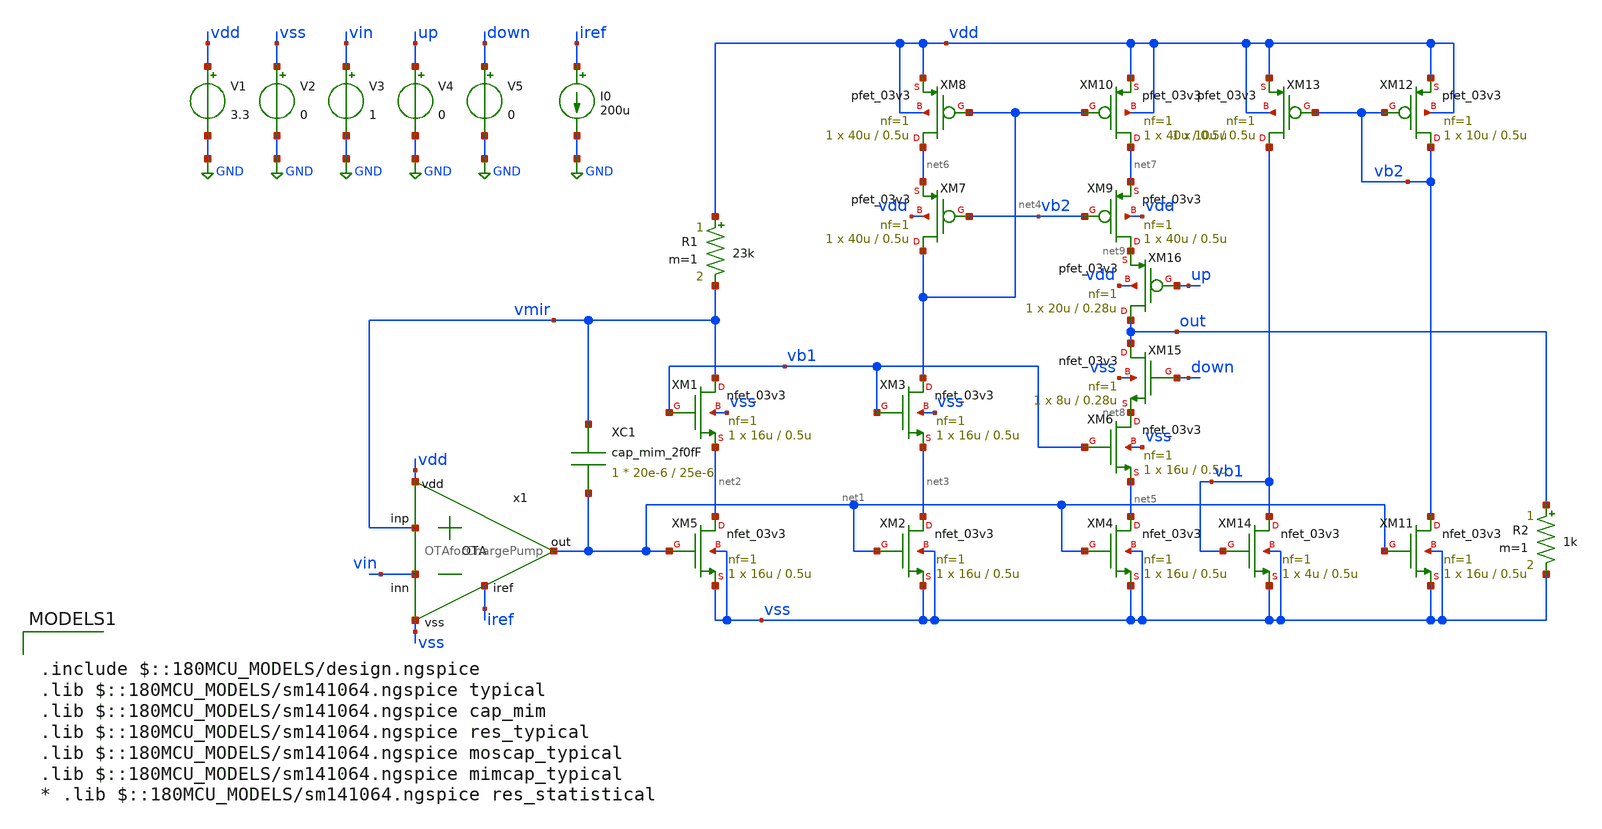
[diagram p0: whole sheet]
** sch_path: designs/libs/qw_core_analog_pkedit/VCOCP/VCOCP.sch
**.subckt VCOCP
x1 vdd iref vmir vin net1 vss OTAforChargePump
XM5 net2 net1 vss vss nfet_03v3 L=0.5u W=16u nf=1 ad='int((nf+1)/2) * W/nf * 0.18u' as='int((nf+2)/2) * W/nf * 0.18u'
+ pd='2*int((nf+1)/2) * (W/nf + 0.18u)' ps='2*int((nf+2)/2) * (W/nf + 0.18u)' nrd='0.18u / W' nrs='0.18u / W'
+ sa=0 sb=0 sd=0 m=1
XM1 vmir vb1 net2 vss nfet_03v3 L=0.5u W=16u nf=1 ad='int((nf+1)/2) * W/nf * 0.18u' as='int((nf+2)/2) * W/nf * 0.18u'
+ pd='2*int((nf+1)/2) * (W/nf + 0.18u)' ps='2*int((nf+2)/2) * (W/nf + 0.18u)' nrd='0.18u / W' nrs='0.18u / W'
+ sa=0 sb=0 sd=0 m=1
XM2 net3 net1 vss vss nfet_03v3 L=0.5u W=16u nf=1 ad='int((nf+1)/2) * W/nf * 0.18u' as='int((nf+2)/2) * W/nf * 0.18u'
+ pd='2*int((nf+1)/2) * (W/nf + 0.18u)' ps='2*int((nf+2)/2) * (W/nf + 0.18u)' nrd='0.18u / W' nrs='0.18u / W'
+ sa=0 sb=0 sd=0 m=1
XM3 net4 vb1 net3 vss nfet_03v3 L=0.5u W=16u nf=1 ad='int((nf+1)/2) * W/nf * 0.18u' as='int((nf+2)/2) * W/nf * 0.18u'
+ pd='2*int((nf+1)/2) * (W/nf + 0.18u)' ps='2*int((nf+2)/2) * (W/nf + 0.18u)' nrd='0.18u / W' nrs='0.18u / W'
+ sa=0 sb=0 sd=0 m=1
XM4 net5 net1 vss vss nfet_03v3 L=0.5u W=16u nf=1 ad='int((nf+1)/2) * W/nf * 0.18u' as='int((nf+2)/2) * W/nf * 0.18u'
+ pd='2*int((nf+1)/2) * (W/nf + 0.18u)' ps='2*int((nf+2)/2) * (W/nf + 0.18u)' nrd='0.18u / W' nrs='0.18u / W'
+ sa=0 sb=0 sd=0 m=1
XM6 net8 vb1 net5 vss nfet_03v3 L=0.5u W=16u nf=1 ad='int((nf+1)/2) * W/nf * 0.18u' as='int((nf+2)/2) * W/nf * 0.18u'
+ pd='2*int((nf+1)/2) * (W/nf + 0.18u)' ps='2*int((nf+2)/2) * (W/nf + 0.18u)' nrd='0.18u / W' nrs='0.18u / W'
+ sa=0 sb=0 sd=0 m=1
XM7 net4 vb2 net6 vdd pfet_03v3 L=0.5u W=40u nf=1 ad='int((nf+1)/2) * W/nf * 0.18u' as='int((nf+2)/2) * W/nf * 0.18u'
+ pd='2*int((nf+1)/2) * (W/nf + 0.18u)' ps='2*int((nf+2)/2) * (W/nf + 0.18u)' nrd='0.18u / W' nrs='0.18u / W'
+ sa=0 sb=0 sd=0 m=1
XM8 net6 net4 vdd vdd pfet_03v3 L=0.5u W=40u nf=1 ad='int((nf+1)/2) * W/nf * 0.18u' as='int((nf+2)/2) * W/nf * 0.18u'
+ pd='2*int((nf+1)/2) * (W/nf + 0.18u)' ps='2*int((nf+2)/2) * (W/nf + 0.18u)' nrd='0.18u / W' nrs='0.18u / W'
+ sa=0 sb=0 sd=0 m=1
XM9 net9 vb2 net7 vdd pfet_03v3 L=0.5u W=40u nf=1 ad='int((nf+1)/2) * W/nf * 0.18u' as='int((nf+2)/2) * W/nf * 0.18u'
+ pd='2*int((nf+1)/2) * (W/nf + 0.18u)' ps='2*int((nf+2)/2) * (W/nf + 0.18u)' nrd='0.18u / W' nrs='0.18u / W'
+ sa=0 sb=0 sd=0 m=1
XM10 net7 net4 vdd vdd pfet_03v3 L=0.5u W=40u nf=1 ad='int((nf+1)/2) * W/nf * 0.18u' as='int((nf+2)/2) * W/nf * 0.18u'
+ pd='2*int((nf+1)/2) * (W/nf + 0.18u)' ps='2*int((nf+2)/2) * (W/nf + 0.18u)' nrd='0.18u / W' nrs='0.18u / W'
+ sa=0 sb=0 sd=0 m=1
R1 vdd vmir 23k m=1
XM11 vb2 net1 vss vss nfet_03v3 L=0.5u W=16u nf=1 ad='int((nf+1)/2) * W/nf * 0.18u' as='int((nf+2)/2) * W/nf * 0.18u'
+ pd='2*int((nf+1)/2) * (W/nf + 0.18u)' ps='2*int((nf+2)/2) * (W/nf + 0.18u)' nrd='0.18u / W' nrs='0.18u / W'
+ sa=0 sb=0 sd=0 m=1
XM12 vb2 vb2 vdd vdd pfet_03v3 L=0.5u W=10u nf=1 ad='int((nf+1)/2) * W/nf * 0.18u' as='int((nf+2)/2) * W/nf * 0.18u'
+ pd='2*int((nf+1)/2) * (W/nf + 0.18u)' ps='2*int((nf+2)/2) * (W/nf + 0.18u)' nrd='0.18u / W' nrs='0.18u / W'
+ sa=0 sb=0 sd=0 m=1
XM13 vb1 vb2 vdd vdd pfet_03v3 L=0.5u W=10u nf=1 ad='int((nf+1)/2) * W/nf * 0.18u' as='int((nf+2)/2) * W/nf * 0.18u'
+ pd='2*int((nf+1)/2) * (W/nf + 0.18u)' ps='2*int((nf+2)/2) * (W/nf + 0.18u)' nrd='0.18u / W' nrs='0.18u / W'
+ sa=0 sb=0 sd=0 m=1
XM14 vb1 vb1 vss vss nfet_03v3 L=0.5u W=4u nf=1 ad='int((nf+1)/2) * W/nf * 0.18u' as='int((nf+2)/2) * W/nf * 0.18u'
+ pd='2*int((nf+1)/2) * (W/nf + 0.18u)' ps='2*int((nf+2)/2) * (W/nf + 0.18u)' nrd='0.18u / W' nrs='0.18u / W'
+ sa=0 sb=0 sd=0 m=1
XM15 out down net8 vss nfet_03v3 L=0.28u W=8u nf=1 ad='int((nf+1)/2) * W/nf * 0.18u' as='int((nf+2)/2) * W/nf * 0.18u'
+ pd='2*int((nf+1)/2) * (W/nf + 0.18u)' ps='2*int((nf+2)/2) * (W/nf + 0.18u)' nrd='0.18u / W' nrs='0.18u / W'
+ sa=0 sb=0 sd=0 m=1
XM16 out up net9 vdd pfet_03v3 L=0.28u W=20u nf=1 ad='int((nf+1)/2) * W/nf * 0.18u' as='int((nf+2)/2) * W/nf * 0.18u'
+ pd='2*int((nf+1)/2) * (W/nf + 0.18u)' ps='2*int((nf+2)/2) * (W/nf + 0.18u)' nrd='0.18u / W' nrs='0.18u / W'
+ sa=0 sb=0 sd=0 m=1
R2 out vss 1k m=1
V1 vdd GND 3.3
V2 vss GND 0
V3 vin GND 1
V4 up GND 0
V5 down GND 0
I0 iref GND 200u
XC1 vmir net1 cap_mim_2f0fF c_width=20e-6 c_length=25e-6 m=1
**** begin user architecture code


.control
save all

**OP
**show all > op.log
**show all

** Source settings
**alter @V5[PULSE] = [ 1.64 1.66 20n 0.1n 0.1n 19.98n 40n 0 ]
**alter @V4[PULSE] = [ 1.66 1.64 20n 0.1n 0.1n 19.98n 40n 0 ]
**alter @V3[PULSE] = [ 0 3.3 10n 0.1n 0.1n 9.98n 20n 0 ]
**alter @V4[PULSE] = [ 0 3.3 50u 0.1u 0.1u 49.8u 100u 0 ]
**alter @V3[PULSE] = [ 0 3.3 75u 0.1u 0.1u 49.8u 100u 0 ]

** Initial Conditions
**C1 up 0 1u IC = 0
**C2 down 0 10f IC = 0

** Simulation settings
**.tran 1n 50u UIC
tran 1p 10n

write VCOCP.raw
.endc



.include $::180MCU_MODELS/design.ngspice
.lib $::180MCU_MODELS/sm141064.ngspice typical
.lib $::180MCU_MODELS/sm141064.ngspice cap_mim
.lib $::180MCU_MODELS/sm141064.ngspice res_typical
.lib $::180MCU_MODELS/sm141064.ngspice moscap_typical
.lib $::180MCU_MODELS/sm141064.ngspice mimcap_typical
* .lib $::180MCU_MODELS/sm141064.ngspice res_statistical

**** end user architecture code
**.ends

* expanding   symbol:  libs/qw_core_analog/OTAforChargePump/OTAforChargePump.sym # of pins=6
** sym_path: designs/libs/qw_core_analog_pkedit/OTAforChargePump/OTAforChargePump.sym
** sch_path: designs/libs/qw_core_analog_pkedit/OTAforChargePump/OTAforChargePump.sch
.subckt OTAforChargePump vdd iref inp inn out vss
*.iopin inp
*.iopin inn
*.iopin vdd
*.iopin vss
*.iopin out
*.iopin iref
XM8 iref iref vdd vdd pfet_03v3 L=0.28u W=40u nf=1 ad='int((nf+1)/2) * W/nf * 0.18u' as='int((nf+2)/2) * W/nf * 0.18u'
+ pd='2*int((nf+1)/2) * (W/nf + 0.18u)' ps='2*int((nf+2)/2) * (W/nf + 0.18u)' nrd='0.18u / W' nrs='0.18u / W'
+ sa=0 sb=0 sd=0 m=1
XM1 net1 iref vdd vdd pfet_03v3 L=0.28u W=40u nf=1 ad='int((nf+1)/2) * W/nf * 0.18u' as='int((nf+2)/2) * W/nf * 0.18u'
+ pd='2*int((nf+1)/2) * (W/nf + 0.18u)' ps='2*int((nf+2)/2) * (W/nf + 0.18u)' nrd='0.18u / W' nrs='0.18u / W'
+ sa=0 sb=0 sd=0 m=1
XM2 net2 inp net1 vdd pfet_03v3 L=0.28u W=20u nf=1 ad='int((nf+1)/2) * W/nf * 0.18u' as='int((nf+2)/2) * W/nf * 0.18u'
+ pd='2*int((nf+1)/2) * (W/nf + 0.18u)' ps='2*int((nf+2)/2) * (W/nf + 0.18u)' nrd='0.18u / W' nrs='0.18u / W'
+ sa=0 sb=0 sd=0 m=1
XM3 out inn net1 vdd pfet_03v3 L=0.28u W=20u nf=1 ad='int((nf+1)/2) * W/nf * 0.18u' as='int((nf+2)/2) * W/nf * 0.18u'
+ pd='2*int((nf+1)/2) * (W/nf + 0.18u)' ps='2*int((nf+2)/2) * (W/nf + 0.18u)' nrd='0.18u / W' nrs='0.18u / W'
+ sa=0 sb=0 sd=0 m=1
XM4 net2 net2 vss vss nfet_03v3 L=0.28u W=8u nf=1 ad='int((nf+1)/2) * W/nf * 0.18u' as='int((nf+2)/2) * W/nf * 0.18u'
+ pd='2*int((nf+1)/2) * (W/nf + 0.18u)' ps='2*int((nf+2)/2) * (W/nf + 0.18u)' nrd='0.18u / W' nrs='0.18u / W'
+ sa=0 sb=0 sd=0 m=1
XM5 out net2 vss vss nfet_03v3 L=0.28u W=8u nf=1 ad='int((nf+1)/2) * W/nf * 0.18u' as='int((nf+2)/2) * W/nf * 0.18u'
+ pd='2*int((nf+1)/2) * (W/nf + 0.18u)' ps='2*int((nf+2)/2) * (W/nf + 0.18u)' nrd='0.18u / W' nrs='0.18u / W'
+ sa=0 sb=0 sd=0 m=1
.ends

.GLOBAL GND
.end
